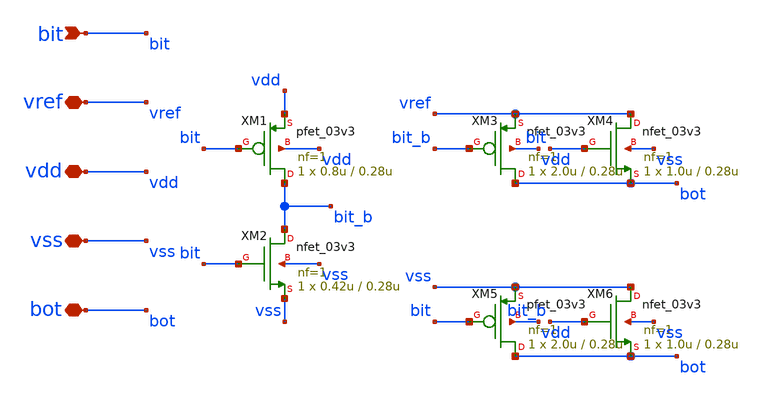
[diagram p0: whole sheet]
** sch_path: xschem/sar_adc/blocks/cdac/cdac_switch_1b.sch
**.subckt cdac_switch_1b bit vref vdd vss bot
*.ipin bit
*.iopin vref
*.iopin vdd
*.iopin vss
*.iopin bot
XM1 bit_b bit vdd vdd pfet_03v3 L=0.28u W=0.8u nf=1 ad='int((nf+1)/2) * W/nf * 0.18u' as='int((nf+2)/2) * W/nf * 0.18u'
+ pd='2*int((nf+1)/2) * (W/nf + 0.18u)' ps='2*int((nf+2)/2) * (W/nf + 0.18u)' nrd='0.18u / W' nrs='0.18u / W'
+ sa=0 sb=0 sd=0 m=1
XM2 bit_b bit vss vss nfet_03v3 L=0.28u W=0.42u nf=1 ad='int((nf+1)/2) * W/nf * 0.18u' as='int((nf+2)/2) * W/nf * 0.18u'
+ pd='2*int((nf+1)/2) * (W/nf + 0.18u)' ps='2*int((nf+2)/2) * (W/nf + 0.18u)' nrd='0.18u / W' nrs='0.18u / W'
+ sa=0 sb=0 sd=0 m=1
XM3 bot bit_b vref vdd pfet_03v3 L=0.28u W=2.0u nf=1 ad='int((nf+1)/2) * W/nf * 0.18u' as='int((nf+2)/2) * W/nf * 0.18u'
+ pd='2*int((nf+1)/2) * (W/nf + 0.18u)' ps='2*int((nf+2)/2) * (W/nf + 0.18u)' nrd='0.18u / W' nrs='0.18u / W'
+ sa=0 sb=0 sd=0 m=1
XM4 vref bit bot vss nfet_03v3 L=0.28u W=1.0u nf=1 ad='int((nf+1)/2) * W/nf * 0.18u' as='int((nf+2)/2) * W/nf * 0.18u'
+ pd='2*int((nf+1)/2) * (W/nf + 0.18u)' ps='2*int((nf+2)/2) * (W/nf + 0.18u)' nrd='0.18u / W' nrs='0.18u / W'
+ sa=0 sb=0 sd=0 m=1
XM5 bot bit vss vdd pfet_03v3 L=0.28u W=2.0u nf=1 ad='int((nf+1)/2) * W/nf * 0.18u' as='int((nf+2)/2) * W/nf * 0.18u'
+ pd='2*int((nf+1)/2) * (W/nf + 0.18u)' ps='2*int((nf+2)/2) * (W/nf + 0.18u)' nrd='0.18u / W' nrs='0.18u / W'
+ sa=0 sb=0 sd=0 m=1
XM6 vss bit_b bot vss nfet_03v3 L=0.28u W=1.0u nf=1 ad='int((nf+1)/2) * W/nf * 0.18u' as='int((nf+2)/2) * W/nf * 0.18u'
+ pd='2*int((nf+1)/2) * (W/nf + 0.18u)' ps='2*int((nf+2)/2) * (W/nf + 0.18u)' nrd='0.18u / W' nrs='0.18u / W'
+ sa=0 sb=0 sd=0 m=1
**.ends
.end
